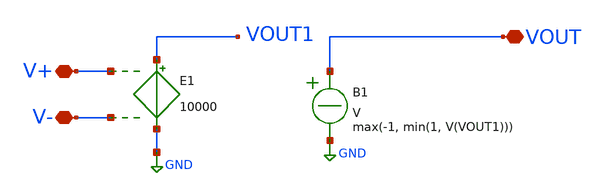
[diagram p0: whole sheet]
** sch_path: Design/Idead_opamp.sch
**.subckt Idead_opamp V- V+ VOUT
*.iopin V-
*.iopin V+
*.iopin VOUT
E1 VOUT1 GND V+ V- 10000
B1 VOUT GND V = max(-1, min(1, V(VOUT1)))
**.ends
.GLOBAL GND
.end
